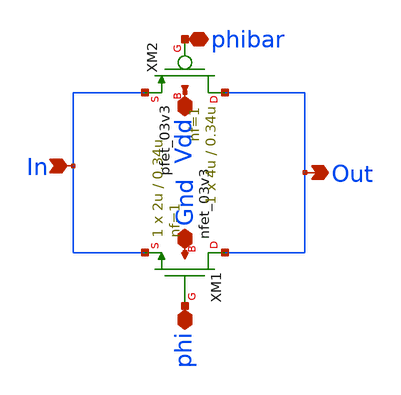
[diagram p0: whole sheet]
** sch_path: xschem/c2v_frontend/TG.sch
**.subckt TG In Out phi phibar Vdd Gnd
*.ipin In
*.opin Out
*.iopin phi
*.iopin phibar
*.iopin Vdd
*.iopin Gnd
XM1 Out phi In Gnd nfet_03v3 L=0.34u W=2u nf=1 ad='int((nf+1)/2) * W/nf * 0.18u' as='int((nf+2)/2) * W/nf * 0.18u'
+ pd='2*int((nf+1)/2) * (W/nf + 0.18u)' ps='2*int((nf+2)/2) * (W/nf + 0.18u)' nrd='0.18u / W' nrs='0.18u / W'
+ sa=0 sb=0 sd=0 m=1
XM2 Out phibar In Vdd pfet_03v3 L=0.34u W=4u nf=1 ad='int((nf+1)/2) * W/nf * 0.18u' as='int((nf+2)/2) * W/nf * 0.18u'
+ pd='2*int((nf+1)/2) * (W/nf + 0.18u)' ps='2*int((nf+2)/2) * (W/nf + 0.18u)' nrd='0.18u / W' nrs='0.18u / W'
+ sa=0 sb=0 sd=0 m=1
**.ends
.end
